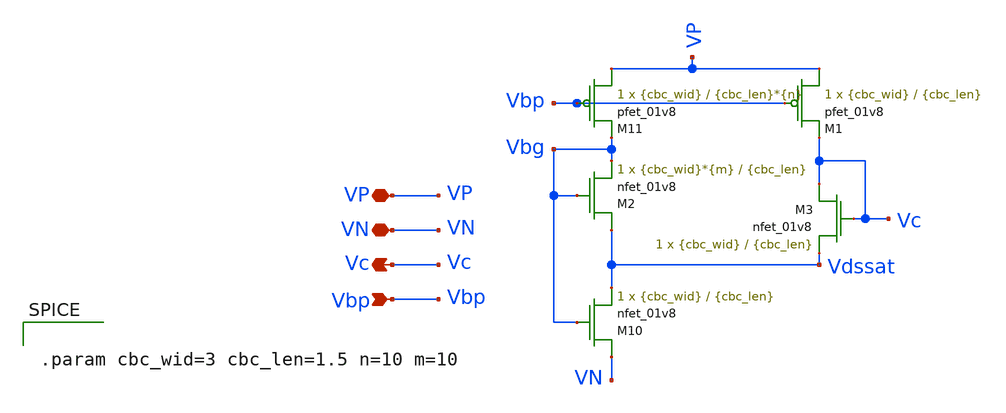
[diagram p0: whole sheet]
** sch_path: ncbc.sch
**.subckt ncbc VP VN Vc Vbp
*.iopin VP
*.iopin VN
*.opin Vc
*.ipin Vbp
XM10 VN Vbg Vdssat VN sky130_fd_pr__nfet_01v8 L={cbc_len} W={cbc_wid} nf=1 ad='int((nf+1)/2) * W/nf * 0.29'
+ as='int((nf+2)/2) * W/nf * 0.29' pd='2*int((nf+1)/2) * (W/nf + 0.29)' ps='2*int((nf+2)/2) * (W/nf + 0.29)'
+ nrd='0.29 / W' nrs='0.29 / W' sa=0 sb=0 sd=0 mult=1 m=1
XM11 VP Vbp Vbg VP sky130_fd_pr__pfet_01v8 L={cbc_len}*{n} W={cbc_wid} nf=1 ad='int((nf+1)/2) * W/nf * 0.29'
+ as='int((nf+2)/2) * W/nf * 0.29' pd='2*int((nf+1)/2) * (W/nf + 0.29)' ps='2*int((nf+2)/2) * (W/nf + 0.29)'
+ nrd='0.29 / W' nrs='0.29 / W' sa=0 sb=0 sd=0 mult=1 m=1
XM1 VP Vbp Vc VP sky130_fd_pr__pfet_01v8 L={cbc_len} W={cbc_wid} nf=1 ad='int((nf+1)/2) * W/nf * 0.29'
+ as='int((nf+2)/2) * W/nf * 0.29' pd='2*int((nf+1)/2) * (W/nf + 0.29)' ps='2*int((nf+2)/2) * (W/nf + 0.29)'
+ nrd='0.29 / W' nrs='0.29 / W' sa=0 sb=0 sd=0 mult=1 m=1
XM2 Vdssat Vbg Vbg VN sky130_fd_pr__nfet_01v8 L={cbc_len} W={cbc_wid}*{m} nf=1 ad='int((nf+1)/2) * W/nf * 0.29'
+ as='int((nf+2)/2) * W/nf * 0.29' pd='2*int((nf+1)/2) * (W/nf + 0.29)' ps='2*int((nf+2)/2) * (W/nf + 0.29)'
+ nrd='0.29 / W' nrs='0.29 / W' sa=0 sb=0 sd=0 mult=1 m=1
XM3 Vc Vc Vdssat VN sky130_fd_pr__nfet_01v8 L={cbc_len} W={cbc_wid} nf=1 ad='int((nf+1)/2) * W/nf * 0.29'
+ as='int((nf+2)/2) * W/nf * 0.29' pd='2*int((nf+1)/2) * (W/nf + 0.29)' ps='2*int((nf+2)/2) * (W/nf + 0.29)'
+ nrd='0.29 / W' nrs='0.29 / W' sa=0 sb=0 sd=0 mult=1 m=1
**** begin user architecture code


.param cbc_wid=3 cbc_len=1.5 n=10 m=10


**** end user architecture code
**.ends
.end
